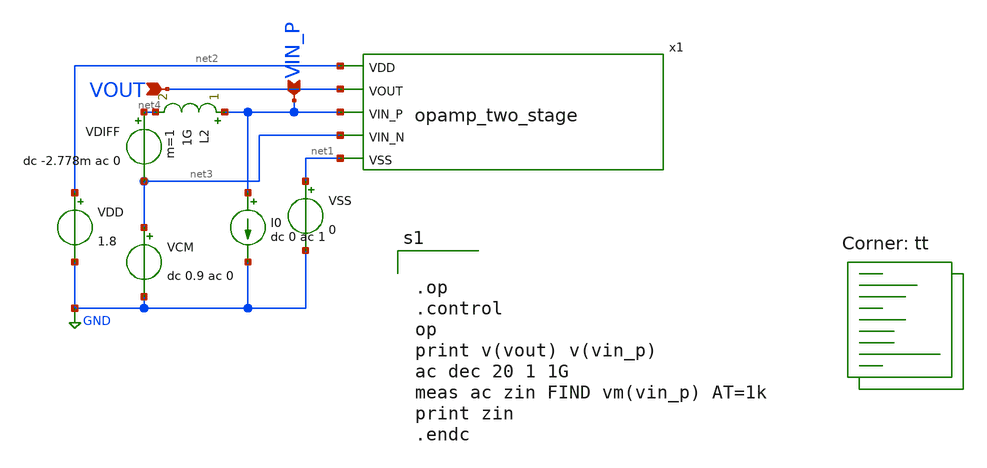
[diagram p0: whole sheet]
** sch_path: analog/bootcamp_opamp/schematics/tb_zin.sch
**.subckt tb_zin VOUT VIN_P
*.ipin VOUT
*.ipin VIN_P
VDD net2 GND 1.8
VSS net1 GND 0
VCM net3 GND dc 0.9 ac 0
VDIFF net4 net3 dc -2.778m ac 0
x1 net2 VOUT VIN_P net3 net1 opamp_two_stage
I0 VIN_P GND dc 0 ac 1
L2 VIN_P net4 1G m=1
**** begin user architecture code


.op
.control
op
print v(vout) v(vin_p)
ac dec 20 1 1G
meas ac zin FIND vm(vin_p) AT=1k
print zin
.endc

.lib $::SKYWATER_MODELS/sky130.lib.spice tt
**** end user architecture code
**.ends

* expanding   symbol:  opamp_two_stage.sym # of pins=5
** sym_path: analog/bootcamp_opamp/schematics/opamp_two_stage.sym
** sch_path: analog/bootcamp_opamp/schematics/opamp_two_stage.sch
.subckt opamp_two_stage VDD VOUT VIN_P VIN_N VSS
*.ipin VIN_N
*.ipin VIN_P
*.ipin VDD
*.ipin VSS
*.ipin VOUT
XMN1 net2 VIN_N net1 VSS sky130_fd_pr__nfet_01v8 L=1 W=20 nf=1 ad='int((nf+1)/2) * W/nf * 0.29' as='int((nf+2)/2) * W/nf * 0.29'
+ pd='2*int((nf+1)/2) * (W/nf + 0.29)' ps='2*int((nf+2)/2) * (W/nf + 0.29)' nrd='0.29 / W' nrs='0.29 / W'
+ sa=0 sb=0 sd=0 mult=1 m=1
XMP1 net2 net2 VDD VDD sky130_fd_pr__pfet_01v8 L=1 W=10 nf=1 ad='int((nf+1)/2) * W/nf * 0.29' as='int((nf+2)/2) * W/nf * 0.29'
+ pd='2*int((nf+1)/2) * (W/nf + 0.29)' ps='2*int((nf+2)/2) * (W/nf + 0.29)' nrd='0.29 / W' nrs='0.29 / W'
+ sa=0 sb=0 sd=0 mult=1 m=1
XMP2 net3 net2 VDD VDD sky130_fd_pr__pfet_01v8 L=1 W=10 nf=1 ad='int((nf+1)/2) * W/nf * 0.29' as='int((nf+2)/2) * W/nf * 0.29'
+ pd='2*int((nf+1)/2) * (W/nf + 0.29)' ps='2*int((nf+2)/2) * (W/nf + 0.29)' nrd='0.29 / W' nrs='0.29 / W'
+ sa=0 sb=0 sd=0 mult=1 m=1
XMN2 net3 VIN_P net1 VSS sky130_fd_pr__nfet_01v8 L=1 W=20 nf=1 ad='int((nf+1)/2) * W/nf * 0.29' as='int((nf+2)/2) * W/nf * 0.29'
+ pd='2*int((nf+1)/2) * (W/nf + 0.29)' ps='2*int((nf+2)/2) * (W/nf + 0.29)' nrd='0.29 / W' nrs='0.29 / W'
+ sa=0 sb=0 sd=0 mult=1 m=1
XMNB net1 net5 VSS VSS sky130_fd_pr__nfet_01v8 L=1 W=4 nf=1 ad='int((nf+1)/2) * W/nf * 0.29' as='int((nf+2)/2) * W/nf * 0.29'
+ pd='2*int((nf+1)/2) * (W/nf + 0.29)' ps='2*int((nf+2)/2) * (W/nf + 0.29)' nrd='0.29 / W' nrs='0.29 / W'
+ sa=0 sb=0 sd=0 mult=2 m=2
XMPO VOUT net3 VDD VDD sky130_fd_pr__pfet_01v8 L=0.15 W=15 nf=1 ad='int((nf+1)/2) * W/nf * 0.29' as='int((nf+2)/2) * W/nf * 0.29'
+ pd='2*int((nf+1)/2) * (W/nf + 0.29)' ps='2*int((nf+2)/2) * (W/nf + 0.29)' nrd='0.29 / W' nrs='0.29 / W'
+ sa=0 sb=0 sd=0 mult=8 m=8
XR1 net4 net3 sky130_fd_pr__res_generic_po W=1 L=2.5 m=1
XC1 net4 VOUT sky130_fd_pr__cap_mim_m3_1 W=22 L=22 MF=1 m=1
XMB VOUT net5 VSS VSS sky130_fd_pr__nfet_01v8 L=0.15 W=6 nf=1 ad='int((nf+1)/2) * W/nf * 0.29' as='int((nf+2)/2) * W/nf * 0.29'
+ pd='2*int((nf+1)/2) * (W/nf + 0.29)' ps='2*int((nf+2)/2) * (W/nf + 0.29)' nrd='0.29 / W' nrs='0.29 / W'
+ sa=0 sb=0 sd=0 mult=8 m=8
XR2 net5 VDD VSS sky130_fd_pr__res_xhigh_po_0p69 L=16 mult=1 m=1
XMB1 net5 net5 VSS VSS sky130_fd_pr__nfet_01v8 L=1 W=4 nf=1 ad='int((nf+1)/2) * W/nf * 0.29' as='int((nf+2)/2) * W/nf * 0.29'
+ pd='2*int((nf+1)/2) * (W/nf + 0.29)' ps='2*int((nf+2)/2) * (W/nf + 0.29)' nrd='0.29 / W' nrs='0.29 / W'
+ sa=0 sb=0 sd=0 mult=1 m=1
.ends

.GLOBAL GND
.end
